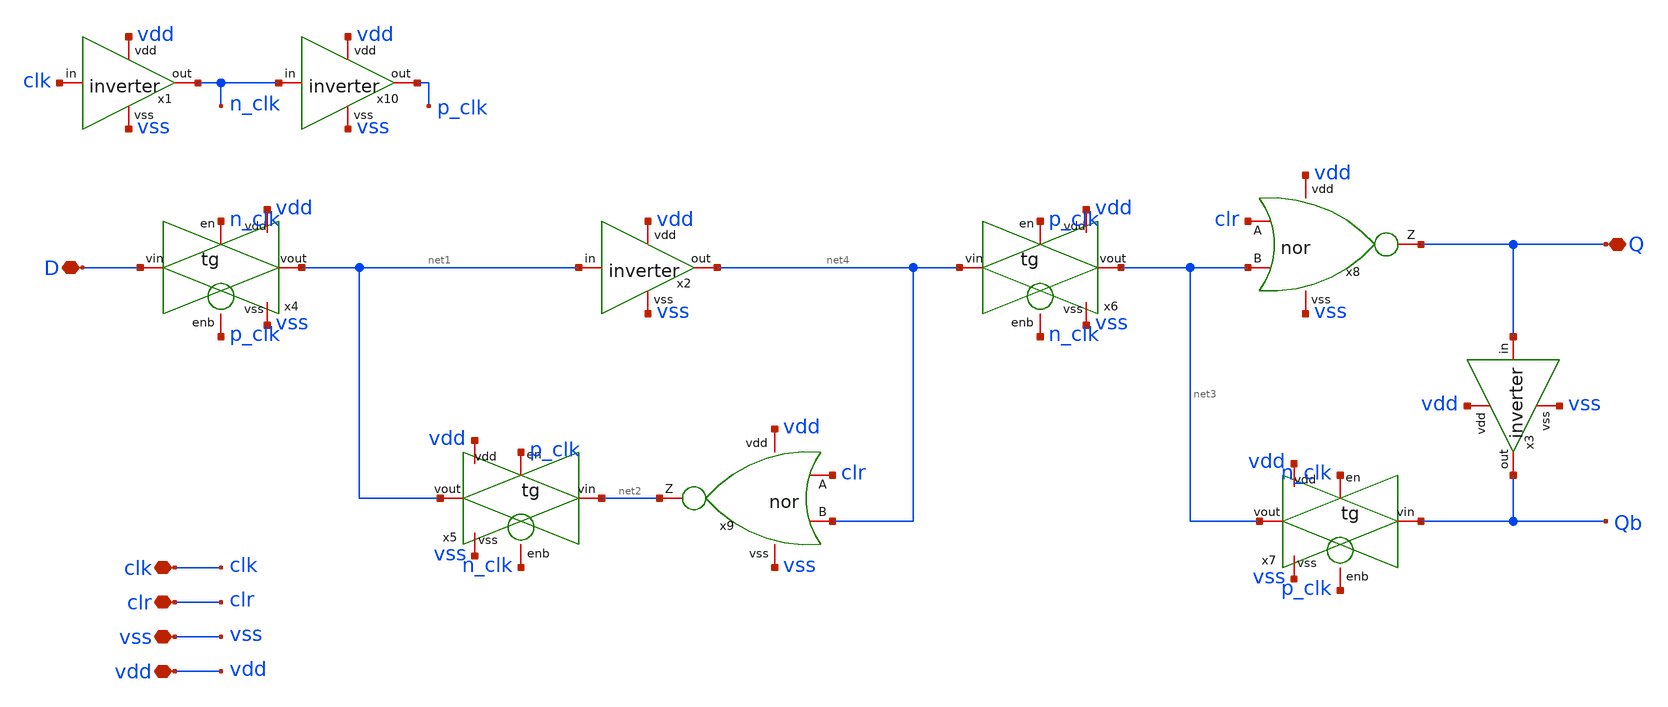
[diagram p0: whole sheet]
** sch_path: designs/sch/dffc.sch
**.subckt dffc clk clr vss vdd D Q
*.iopin clk
*.iopin clr
*.iopin vss
*.iopin vdd
*.iopin D
*.iopin Q
x1 vdd n_clk clk vss inverter
x2 vdd net4 net1 vss inverter
x3 vdd Qb Q vss inverter
x4 D p_clk n_clk net1 vss vdd tg
x8 vdd Q clr net3 vss nor
x9 vdd net2 clr net4 vss nor
x5 net2 n_clk p_clk net1 vss vdd tg
x6 net4 n_clk p_clk net3 vss vdd tg
x7 Qb p_clk n_clk net3 vss vdd tg
x10 vdd p_clk n_clk vss inverter
**.ends
.end
